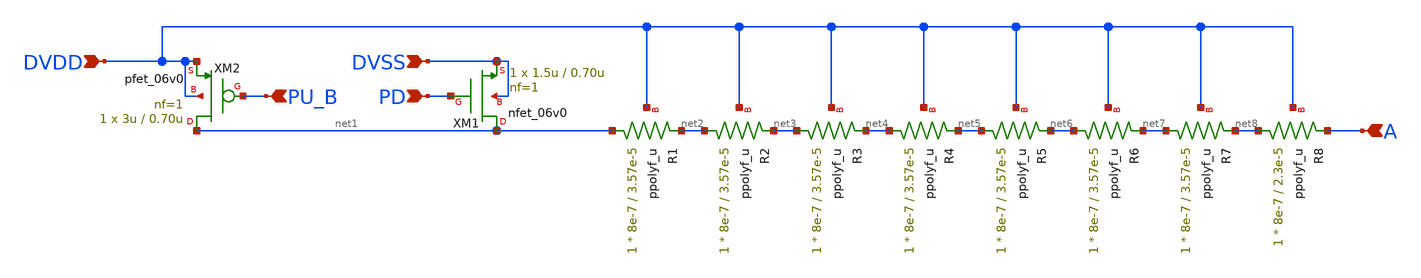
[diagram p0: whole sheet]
** sch_path: gf180mcu_fd_io__bi_24t/comp018green_in_pupd.sch
**.subckt comp018green_in_pupd DVDD DVSS PD PU_B A
*.ipin DVDD
*.ipin DVSS
*.ipin PD
*.ipin PU_B
*.ipin A
XM1 net1 PD DVSS DVSS nfet_06v0 L=0.70u W=1.5u nf=1 ad='int((nf+1)/2) * W/nf * 0.18u' as='int((nf+2)/2) * W/nf * 0.18u'
+ pd='2*int((nf+1)/2) * (W/nf + 0.18u)' ps='2*int((nf+2)/2) * (W/nf + 0.18u)' nrd='0.18u / W' nrs='0.18u / W'
+ sa=0 sb=0 sd=0 m=1
XM2 net1 PU_B DVDD DVDD pfet_06v0 L=0.70u W=3u nf=1 ad='int((nf+1)/2) * W/nf * 0.18u' as='int((nf+2)/2) * W/nf * 0.18u'
+ pd='2*int((nf+1)/2) * (W/nf + 0.18u)' ps='2*int((nf+2)/2) * (W/nf + 0.18u)' nrd='0.18u / W' nrs='0.18u / W'
+ sa=0 sb=0 sd=0 m=1
XR1 net1 net2 DVDD ppolyf_u r_width=8e-7 r_length=3.57e-5 m=1
XR2 net2 net3 DVDD ppolyf_u r_width=8e-7 r_length=3.57e-5 m=1
XR3 net3 net4 DVDD ppolyf_u r_width=8e-7 r_length=3.57e-5 m=1
XR4 net4 net5 DVDD ppolyf_u r_width=8e-7 r_length=3.57e-5 m=1
XR5 net5 net6 DVDD ppolyf_u r_width=8e-7 r_length=3.57e-5 m=1
XR6 net6 net7 DVDD ppolyf_u r_width=8e-7 r_length=3.57e-5 m=1
XR7 net7 net8 DVDD ppolyf_u r_width=8e-7 r_length=3.57e-5 m=1
XR8 net8 A DVDD ppolyf_u r_width=8e-7 r_length=2.3e-5 m=1
**.ends
.end
